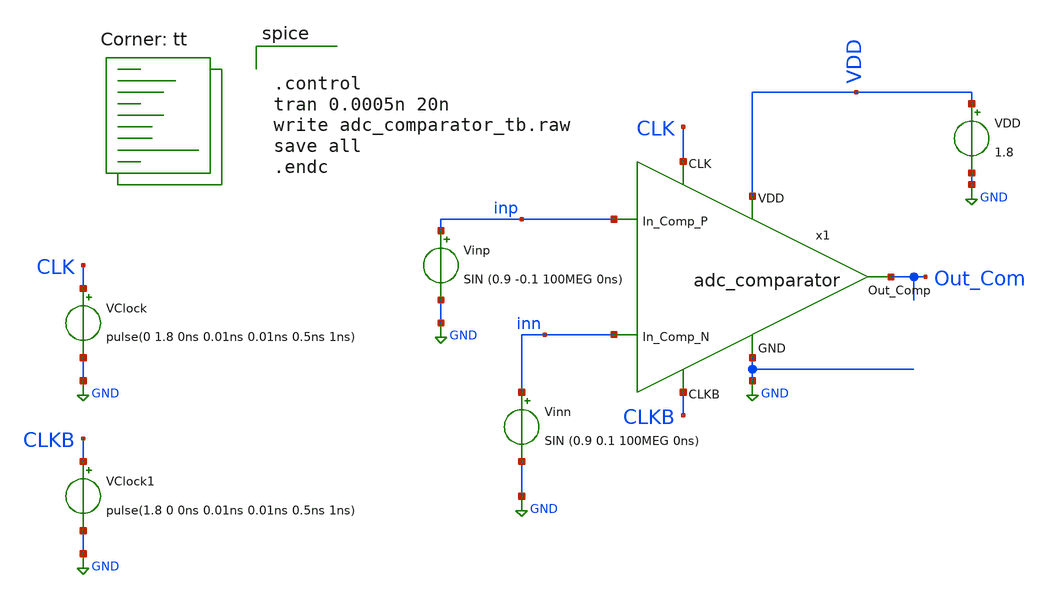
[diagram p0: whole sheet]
** sch_path: adc_comparator_tb.sch
**.subckt adc_comparator_tb
x1 VDD inp inn Out_Com CLK CLKB GND adc_comparator
VDD VDD GND 1.8
VClock CLK GND pulse(0 1.8 0ns 0.01ns 0.01ns 0.5ns 1ns)
Vinp inp GND SIN (0.9 -0.1 100MEG 0ns)
Vinn inn GND SIN (0.9 0.1 100MEG 0ns)
VClock1 CLKB GND pulse(1.8 0 0ns 0.01ns 0.01ns 0.5ns 1ns)
**** begin user architecture code
.lib $::SKYWATER_MODELS/sky130.lib.spice tt


.control
tran 0.0005n 20n
write adc_comparator_tb.raw
save all
.endc

**** end user architecture code
**.ends

* expanding   symbol:  project/adc_comparator.sym # of pins=7
** sym_path: adc_comparator.sym
** sch_path: adc_comparator.sch
.subckt adc_comparator VDD In_Comp_P In_Comp_N Out_Comp CLK CLKB GND
*.ipin VDD
*.ipin GND
*.ipin In_Comp_P
*.ipin In_Comp_N
*.ipin CLK
*.ipin CLKB
*.opin Out_Comp
XM1 O_n CLK VDD VDD sky130_fd_pr__pfet_01v8 L=0.15 W=1 nf=1 ad='int((nf+1)/2) * W/nf * 0.29' as='int((nf+2)/2) * W/nf * 0.29'
+ pd='2*int((nf+1)/2) * (W/nf + 0.29)' ps='2*int((nf+2)/2) * (W/nf + 0.29)' nrd='0.29 / W' nrs='0.29 / W'
+ sa=0 sb=0 sd=0 mult=1 m=1
XM2 O_p CLK VDD VDD sky130_fd_pr__pfet_01v8 L=0.15 W=1 nf=1 ad='int((nf+1)/2) * W/nf * 0.29' as='int((nf+2)/2) * W/nf * 0.29'
+ pd='2*int((nf+1)/2) * (W/nf + 0.29)' ps='2*int((nf+2)/2) * (W/nf + 0.29)' nrd='0.29 / W' nrs='0.29 / W'
+ sa=0 sb=0 sd=0 mult=1 m=1
XM3 net2 Out_Comp VDD VDD sky130_fd_pr__pfet_01v8 L=0.15 W=10 nf=1 ad='int((nf+1)/2) * W/nf * 0.29' as='int((nf+2)/2) * W/nf * 0.29'
+ pd='2*int((nf+1)/2) * (W/nf + 0.29)' ps='2*int((nf+2)/2) * (W/nf + 0.29)' nrd='0.29 / W' nrs='0.29 / W'
+ sa=0 sb=0 sd=0 mult=1 m=1
XM4 net3 net4 VDD VDD sky130_fd_pr__pfet_01v8 L=0.15 W=10 nf=1 ad='int((nf+1)/2) * W/nf * 0.29' as='int((nf+2)/2) * W/nf * 0.29'
+ pd='2*int((nf+1)/2) * (W/nf + 0.29)' ps='2*int((nf+2)/2) * (W/nf + 0.29)' nrd='0.29 / W' nrs='0.29 / W'
+ sa=0 sb=0 sd=0 mult=1 m=1
XM5 net4 O_n net2 VDD sky130_fd_pr__pfet_01v8 L=0.15 W=10 nf=1 ad='int((nf+1)/2) * W/nf * 0.29' as='int((nf+2)/2) * W/nf * 0.29'
+ pd='2*int((nf+1)/2) * (W/nf + 0.29)' ps='2*int((nf+2)/2) * (W/nf + 0.29)' nrd='0.29 / W' nrs='0.29 / W'
+ sa=0 sb=0 sd=0 mult=1 m=1
XM6 Out_Comp O_p net3 VDD sky130_fd_pr__pfet_01v8 L=0.15 W=10 nf=1 ad='int((nf+1)/2) * W/nf * 0.29' as='int((nf+2)/2) * W/nf * 0.29'
+ pd='2*int((nf+1)/2) * (W/nf + 0.29)' ps='2*int((nf+2)/2) * (W/nf + 0.29)' nrd='0.29 / W' nrs='0.29 / W'
+ sa=0 sb=0 sd=0 mult=1 m=1
XM7 O_n In_Comp_P net1 GND sky130_fd_pr__nfet_01v8 L=0.15 W=6.5 nf=1 ad='int((nf+1)/2) * W/nf * 0.29'
+ as='int((nf+2)/2) * W/nf * 0.29' pd='2*int((nf+1)/2) * (W/nf + 0.29)' ps='2*int((nf+2)/2) * (W/nf + 0.29)'
+ nrd='0.29 / W' nrs='0.29 / W' sa=0 sb=0 sd=0 mult=1 m=1
XM8 O_p In_Comp_N net1 GND sky130_fd_pr__nfet_01v8 L=0.15 W=6.5 nf=1 ad='int((nf+1)/2) * W/nf * 0.29'
+ as='int((nf+2)/2) * W/nf * 0.29' pd='2*int((nf+1)/2) * (W/nf + 0.29)' ps='2*int((nf+2)/2) * (W/nf + 0.29)'
+ nrd='0.29 / W' nrs='0.29 / W' sa=0 sb=0 sd=0 mult=1 m=1
XM9 net1 CLK GND GND sky130_fd_pr__nfet_01v8 L=0.15 W=6 nf=1 ad='int((nf+1)/2) * W/nf * 0.29' as='int((nf+2)/2) * W/nf * 0.29'
+ pd='2*int((nf+1)/2) * (W/nf + 0.29)' ps='2*int((nf+2)/2) * (W/nf + 0.29)' nrd='0.29 / W' nrs='0.29 / W'
+ sa=0 sb=0 sd=0 mult=1 m=1
XM10 net4 CLKB GND GND sky130_fd_pr__nfet_01v8 L=0.15 W=1 nf=1 ad='int((nf+1)/2) * W/nf * 0.29' as='int((nf+2)/2) * W/nf * 0.29'
+ pd='2*int((nf+1)/2) * (W/nf + 0.29)' ps='2*int((nf+2)/2) * (W/nf + 0.29)' nrd='0.29 / W' nrs='0.29 / W'
+ sa=0 sb=0 sd=0 mult=1 m=1
XM11 net4 Out_Comp GND GND sky130_fd_pr__nfet_01v8 L=0.15 W=1 nf=1 ad='int((nf+1)/2) * W/nf * 0.29' as='int((nf+2)/2) * W/nf * 0.29'
+ pd='2*int((nf+1)/2) * (W/nf + 0.29)' ps='2*int((nf+2)/2) * (W/nf + 0.29)' nrd='0.29 / W' nrs='0.29 / W'
+ sa=0 sb=0 sd=0 mult=1 m=1
XM12 Out_Comp net4 GND GND sky130_fd_pr__nfet_01v8 L=0.15 W=1 nf=1 ad='int((nf+1)/2) * W/nf * 0.29' as='int((nf+2)/2) * W/nf * 0.29'
+ pd='2*int((nf+1)/2) * (W/nf + 0.29)' ps='2*int((nf+2)/2) * (W/nf + 0.29)' nrd='0.29 / W' nrs='0.29 / W'
+ sa=0 sb=0 sd=0 mult=1 m=1
XM13 Out_Comp CLKB GND GND sky130_fd_pr__nfet_01v8 L=0.15 W=1 nf=1 ad='int((nf+1)/2) * W/nf * 0.29' as='int((nf+2)/2) * W/nf * 0.29'
+ pd='2*int((nf+1)/2) * (W/nf + 0.29)' ps='2*int((nf+2)/2) * (W/nf + 0.29)' nrd='0.29 / W' nrs='0.29 / W'
+ sa=0 sb=0 sd=0 mult=1 m=1
.ends

.GLOBAL GND
.end
